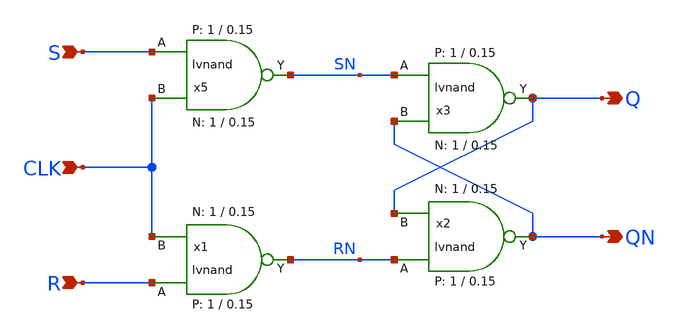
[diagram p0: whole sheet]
** sch_path: sky130A/xschem_libs/sky130_tests_ase/srlatch/schematic/srlatch.sch
* Copyright 2021 Stefan Frederik Schippers
* Licensed under the Apache License, Version 2.0 (the "License");
* you may not use this file except in compliance with the License.
* You may obtain a copy of the License at
* https://www.apache.org/licenses/LICENSE-2.0
* Unless required by applicable law or agreed to in writing, software
* distributed under the License is distributed on an "AS IS" BASIS,
* WITHOUT WARRANTIES OR CONDITIONS OF ANY KIND, either express or implied.
* See the License for the specific language governing permissions and
* limitations under the License.
**.subckt srlatch S R Q QN CLK
*.ipin S
*.ipin R
*.opin Q
*.opin QN
*.ipin CLK
x5 S CLK SN VCC VSS lvnand WidthN=1 LenN=0.15 WidthP=1 LenP=0.15 m=1
x1 R CLK RN VCC VSS lvnand WidthN=1 LenN=0.15 WidthP=1 LenP=0.15 m=1
x2 RN Q QN VCC VSS lvnand WidthN=1 LenN=0.15 WidthP=1 LenP=0.15 m=1
x3 SN QN Q VCC VSS lvnand WidthN=1 LenN=0.15 WidthP=1 LenP=0.15 m=1
**.ends

* expanding   symbol:  sky130_tests/lvnand.sym # of pins=3
** sym_path: sky130_tests/lvnand.sym
** sch_path: sky130_tests/lvnand.sch
.subckt lvnand A B Y VCCPIN VSSPIN  WidthN=1 LenN=0.15 WidthP=1 LenP=0.15
*.ipin A
*.ipin B
*.opin Y
XM1 Y B S VSSPIN sky130_fd_pr__nfet_01v8 L=LenN W=WidthN nf=1 ad='int((nf+1)/2) * W/nf * 0.29' as='int((nf+2)/2) * W/nf * 0.29'
+ pd='2*int((nf+1)/2) * (W/nf + 0.29)' ps='2*int((nf+2)/2) * (W/nf + 0.29)' nrd='0.29 / W' nrs='0.29 / W'
+ sa=0 sb=0 sd=0 mult=1 m=1
XM2 Y A VCCPIN VCCPIN sky130_fd_pr__pfet_01v8 L=LenP W=WidthP nf=1 ad='int((nf+1)/2) * W/nf * 0.29' as='int((nf+2)/2) * W/nf * 0.29'
+ pd='2*int((nf+1)/2) * (W/nf + 0.29)' ps='2*int((nf+2)/2) * (W/nf + 0.29)' nrd='0.29 / W' nrs='0.29 / W'
+ sa=0 sb=0 sd=0 mult=1 m=1
XM3 Y B VCCPIN VCCPIN sky130_fd_pr__pfet_01v8 L=LenP W=WidthP nf=1 ad='int((nf+1)/2) * W/nf * 0.29' as='int((nf+2)/2) * W/nf * 0.29'
+ pd='2*int((nf+1)/2) * (W/nf + 0.29)' ps='2*int((nf+2)/2) * (W/nf + 0.29)' nrd='0.29 / W' nrs='0.29 / W'
+ sa=0 sb=0 sd=0 mult=1 m=1
XM4 S A VSSPIN VSSPIN sky130_fd_pr__nfet_01v8 L=LenN W=WidthN nf=1 ad='int((nf+1)/2) * W/nf * 0.29' as='int((nf+2)/2) * W/nf * 0.29'
+ pd='2*int((nf+1)/2) * (W/nf + 0.29)' ps='2*int((nf+2)/2) * (W/nf + 0.29)' nrd='0.29 / W' nrs='0.29 / W'
+ sa=0 sb=0 sd=0 mult=1 m=1
.ends

.end
